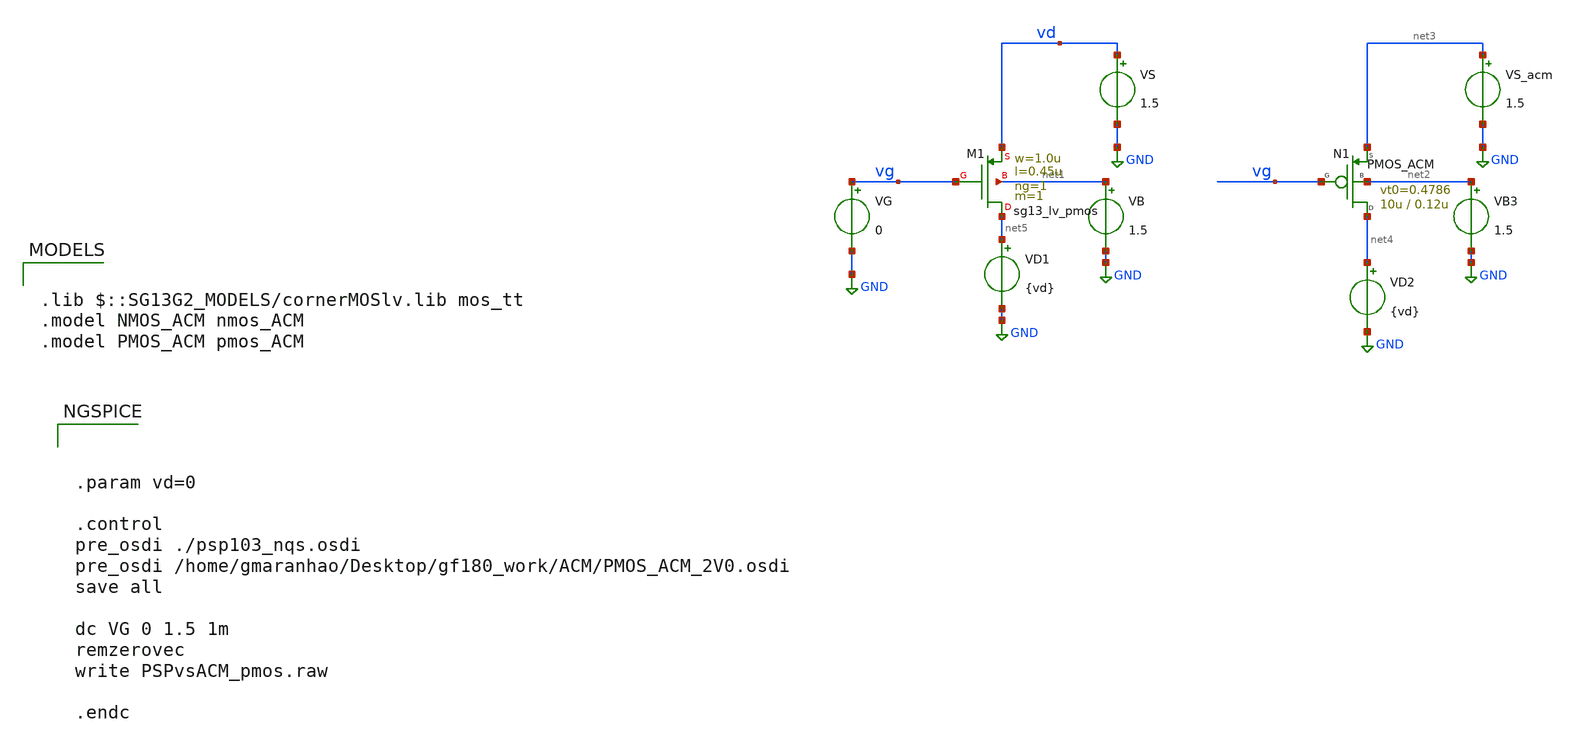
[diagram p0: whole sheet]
** sch_path: ihp_tutorials/PSPvsACM_pmos.sch
**.subckt PSPvsACM_pmos
VG vg GND 0
VD1 net5 GND {vd}
VB net1 GND 1.5
VS vd GND 1.5
VB3 net2 GND 1.5
VS_acm net3 GND 1.5
VD2 net4 GND {vd}
XM1 net5 vg vd net1 sg13_lv_pmos w=1.0u l=0.45u ng=1 m=1 mm_ok=1
N1 net4 vg net3 net2 PMOS_ACM w=10u l=0.12u n=1.466 is=9.391u vt0=0.4786 sigma=48.4m zeta=31m
**** begin user architecture code



.param vd=0

.control
pre_osdi ./psp103_nqs.osdi
pre_osdi /home/gmaranhao/Desktop/gf180_work/ACM/PMOS_ACM_2V0.osdi
save all

dc VG 0 1.5 1m
remzerovec
write PSPvsACM_pmos.raw

.endc



.lib $::SG13G2_MODELS/cornerMOSlv.lib mos_tt
.model NMOS_ACM nmos_ACM
.model PMOS_ACM pmos_ACM

**** end user architecture code
**.ends
.GLOBAL GND
.end
